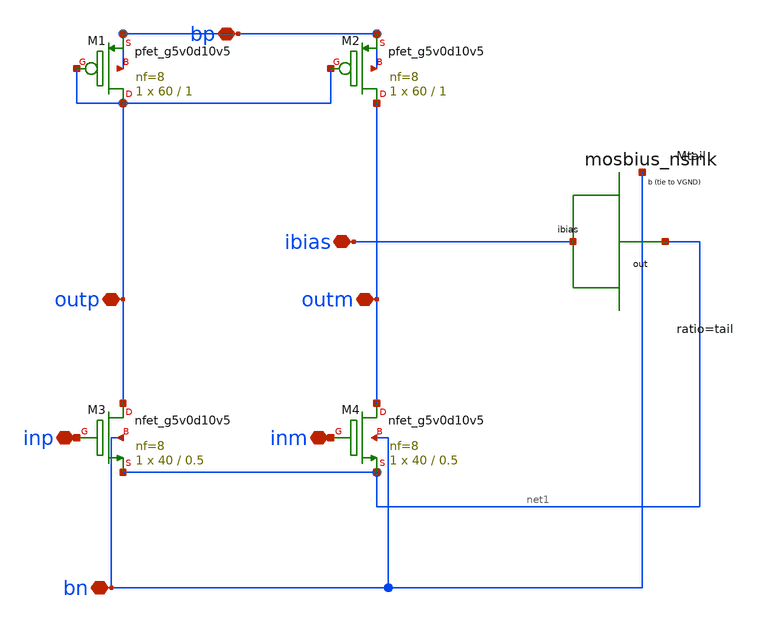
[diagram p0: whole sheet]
** sch_path: xschem/mosbius_lib/mosbius_ota.sch
**.subckt mosbius_ota inp inm outp outm ibias bn bp
*.iopin inp
*.iopin inm
*.iopin outp
*.iopin outm
*.iopin ibias
*.iopin bn
*.iopin bp
XM3 outp inp net1 bn sky130_fd_pr__nfet_g5v0d10v5 L=0.5 W=40 nf=8 ad='int((nf+1)/2) * W/nf * 0.29' as='int((nf+2)/2) * W/nf * 0.29'
+ pd='2*int((nf+1)/2) * (W/nf + 0.29)' ps='2*int((nf+2)/2) * (W/nf + 0.29)' nrd='0.29 / W' nrs='0.29 / W'
+ sa=0 sb=0 sd=0 mult=1 m=1
XM4 outm inm net1 bn sky130_fd_pr__nfet_g5v0d10v5 L=0.5 W=40 nf=8 ad='int((nf+1)/2) * W/nf * 0.29' as='int((nf+2)/2) * W/nf * 0.29'
+ pd='2*int((nf+1)/2) * (W/nf + 0.29)' ps='2*int((nf+2)/2) * (W/nf + 0.29)' nrd='0.29 / W' nrs='0.29 / W'
+ sa=0 sb=0 sd=0 mult=1 m=1
XM1 outp outp bp bp sky130_fd_pr__pfet_g5v0d10v5 L=1 W=60 nf=8 ad='int((nf+1)/2) * W/nf * 0.29' as='int((nf+2)/2) * W/nf * 0.29'
+ pd='2*int((nf+1)/2) * (W/nf + 0.29)' ps='2*int((nf+2)/2) * (W/nf + 0.29)' nrd='0.29 / W' nrs='0.29 / W'
+ sa=0 sb=0 sd=0 mult=1 m=1
XM2 outm outp bp bp sky130_fd_pr__pfet_g5v0d10v5 L=1 W=60 nf=8 ad='int((nf+1)/2) * W/nf * 0.29' as='int((nf+2)/2) * W/nf * 0.29'
+ pd='2*int((nf+1)/2) * (W/nf + 0.29)' ps='2*int((nf+2)/2) * (W/nf + 0.29)' nrd='0.29 / W' nrs='0.29 / W'
+ sa=0 sb=0 sd=0 mult=1 m=1
Mtail ibias net1 bn mosbius_nsink ratio=tail
**.ends

* expanding   symbol:  mosbius_nsink.sym # of pins=3
** sym_path: xschem/mosbius_lib/mosbius_nsink.sym
** sch_path: xschem/mosbius_lib/mosbius_nsink.sch
.subckt mosbius_nsink ibias out b  ratio=1
*.iopin ibias
*.iopin b
*.iopin out
XM1 ibias ibias b b sky130_fd_pr__nfet_g5v0d10v5 L=1 W=10 nf=2 ad='int((nf+1)/2) * W/nf * 0.29' as='int((nf+2)/2) * W/nf * 0.29'
+ pd='2*int((nf+1)/2) * (W/nf + 0.29)' ps='2*int((nf+2)/2) * (W/nf + 0.29)' nrd='0.29 / W' nrs='0.29 / W'
+ sa=0 sb=0 sd=0 mult=1 m=1
XM2 out ibias b b sky130_fd_pr__nfet_g5v0d10v5 L=1 W=10*ratio nf=2*ratio ad='int((nf+1)/2) * W/nf * 0.29'
+ as='int((nf+2)/2) * W/nf * 0.29' pd='2*int((nf+1)/2) * (W/nf + 0.29)' ps='2*int((nf+2)/2) * (W/nf + 0.29)'
+ nrd='0.29 / W' nrs='0.29 / W' sa=0 sb=0 sd=0 mult=1 m=1
.ends

.end
